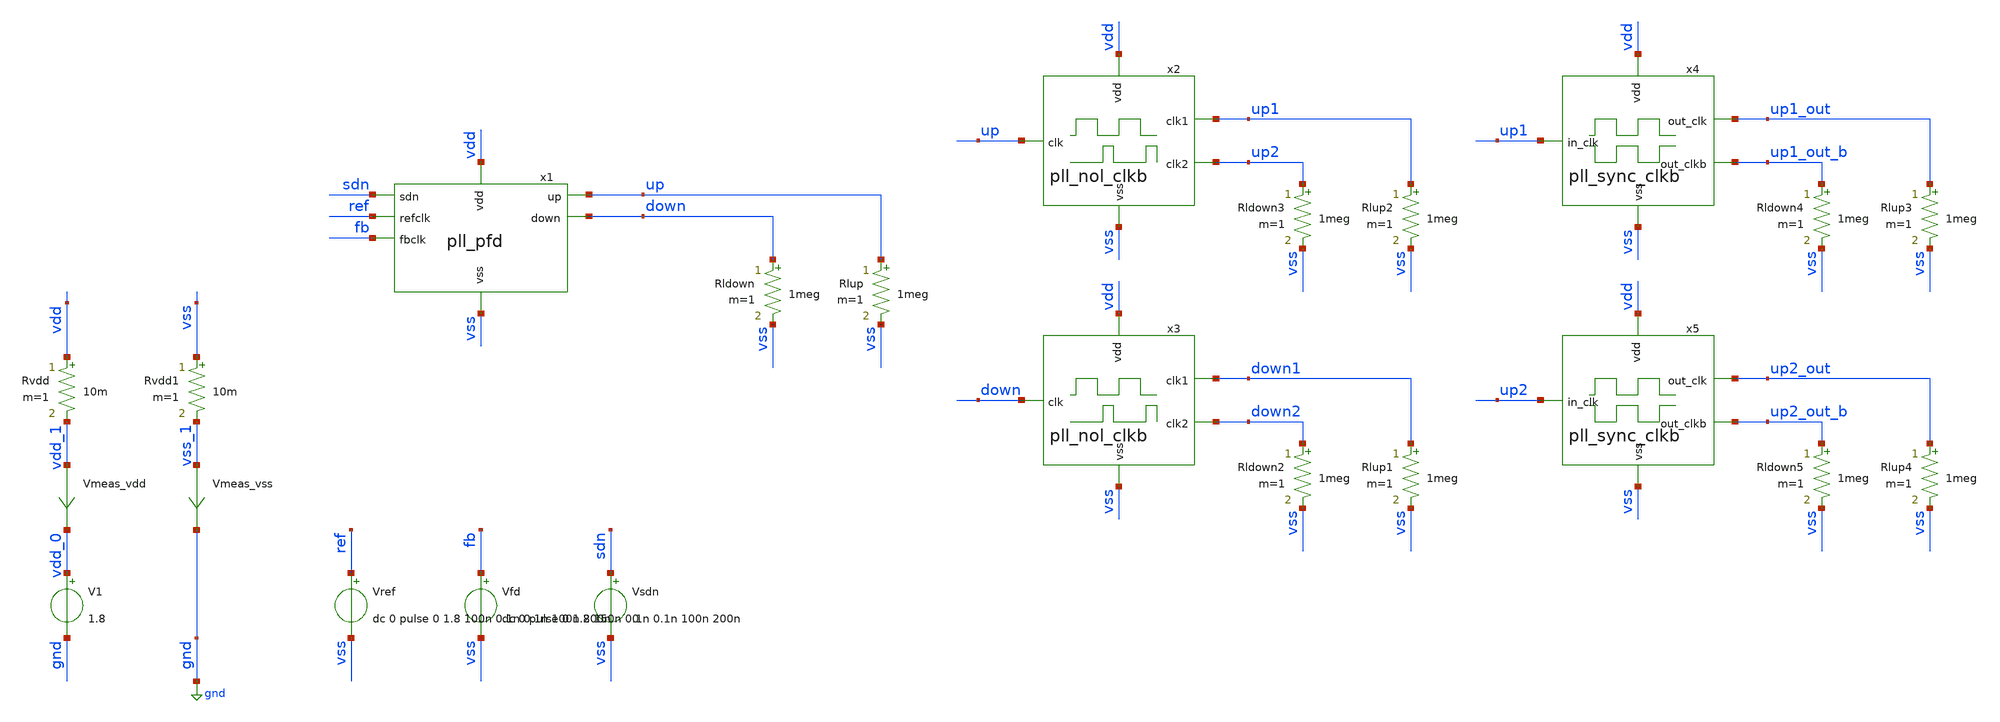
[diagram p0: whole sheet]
** sch_path: pll/pll_pfd/simulation/pll_pfd_tb.sch
**.subckt pll_pfd_tb
V1 vdd_0 gnd 1.8
Vmeas_vdd vdd_1 vdd_0 0
.save i(vmeas_vdd)
Vref ref vss dc 0 pulse 0 1.8 100n 0.1n 0.1n 100n 200n
Vfd fb vss dc 0 pulse 0 1.8 150n 0.1n 0.1n 100n 200n
Vsdn sdn vss 0
Vmeas_vss vss_1 gnd 0
.save i(vmeas_vss)
Rvdd vdd vdd_1 10m m=1
Rvdd1 vss vss_1 10m m=1
Rlup up vss 1meg m=1
Rldown down vss 1meg m=1
Rlup1 down1 vss 1meg m=1
Rldown2 down2 vss 1meg m=1
Rlup2 up1 vss 1meg m=1
Rldown3 up2 vss 1meg m=1
Rlup3 up1_out vss 1meg m=1
Rldown4 up1_out_b vss 1meg m=1
Rlup4 up2_out vss 1meg m=1
Rldown5 up2_out_b vss 1meg m=1
x1 ref up sdn fb down vdd vss pll_pfd
x2 up1 vdd vss up up2 pll_nol_clkb
x3 down1 vdd vss down down2 pll_nol_clkb
x4 up1_out vdd vss up1 up1_out_b pll_sync_clkb
x5 up2_out vdd vss up2 up2_out_b pll_sync_clkb
**** begin user architecture code



*.option savecurrents
*.option rshunt = 1e12
*.option gmin = 1e-24

** Settings for PSS osciallator
*.option reltol=1e-5
*.option vntol=3e-8
*.option abstol=1e-13
**.option chgtol=1e-12
*.option trtol=10
*.option method=gear

.control

* #################################################################
* #
* #                         OPERATING POINT
* #
* #################################################################
reset
save all

op
set filetype=binary
write pll_pfd_tb.raw all

* #################################################################
* #
* #                 TRANSIENT OSCILATION REGIME
* #
* #################################################################
reset
setplot const
save all
save v(ref)
save v(fb)
save v(sdn)
save v(up) v(up1) v(up1_out) v(up1_out_b) v(up2) v(up2_out) v(up2_out_b)
save v(down) v(down1) v(down2)
save v(x2.clkb) v(x2.clk1b) v(x2.clk1fb) v(x2.clk2b) v(x2.clk2fb)
save v(x4.stor_node) v(x4.stor_node_b)

tran 0.05n 1u
set filetype=ascii
write pll_pfd_tb_tran.raw v(ref) v(fb) v(sdn) v(up) v(up1) v(up2) v(down) v(down1) v(down2)

* Plot outputs
plot v(sdn)+16 v(ref)+14 v(fb)+12 v(up)+10 v(up1)+8 v(up2)+6 v(down)+4 v(down1)+2 v(down2)+0
plot v(up1)+10 v(up1_out)+8 v(up1_out_b)+6 v(up2)+4 v(up2_out)+2 v(up2_out_b)+0
plot v(x4.stor_node) v(x4.stor_node_b)

*rusage
.endc



.options wnflag=1
.include $::SKYWATER_MODELS/cells/nfet_01v8/sky130_fd_pr__nfet_01v8__tt.corner.spice
.include $::SKYWATER_MODELS/cells/nfet_01v8_lvt/sky130_fd_pr__nfet_01v8_lvt__tt.corner.spice
.include $::SKYWATER_MODELS/cells/pfet_01v8/sky130_fd_pr__pfet_01v8__tt.corner.spice
.include $::SKYWATER_MODELS/cells/nfet_03v3_nvt/sky130_fd_pr__nfet_03v3_nvt__tt.corner.spice
.include $::SKYWATER_MODELS/cells/nfet_05v0_nvt/sky130_fd_pr__nfet_05v0_nvt__tt.corner.spice
.include $::SKYWATER_MODELS/cells/esd_nfet_01v8/sky130_fd_pr__esd_nfet_01v8__tt.corner.spice
.include $::SKYWATER_MODELS/cells/pfet_01v8_lvt/sky130_fd_pr__pfet_01v8_lvt__tt.corner.spice
.include $::SKYWATER_MODELS/cells/pfet_01v8_hvt/sky130_fd_pr__pfet_01v8_hvt__tt.corner.spice
.include $::SKYWATER_MODELS/cells/esd_pfet_g5v0d10v5/sky130_fd_pr__esd_pfet_g5v0d10v5__tt.corner.spice
.include $::SKYWATER_MODELS/cells/pfet_g5v0d10v5/sky130_fd_pr__pfet_g5v0d10v5__tt.corner.spice
.include $::SKYWATER_MODELS/cells/pfet_g5v0d16v0/sky130_fd_pr__pfet_g5v0d16v0__tt.corner.spice
.include $::SKYWATER_MODELS/cells/nfet_g5v0d10v5/sky130_fd_pr__nfet_g5v0d10v5__tt.corner.spice
.include $::SKYWATER_MODELS/cells/nfet_g5v0d16v0/sky130_fd_pr__nfet_g5v0d16v0__tt_discrete.corner.spice
.include $::SKYWATER_MODELS/cells/esd_nfet_g5v0d10v5/sky130_fd_pr__esd_nfet_g5v0d10v5__tt.corner.spice
.include $::SKYWATER_MODELS/models/corners/tt/nonfet.spice

.include $::SKYWATER_MODELS/cells/cap_var_hvt/sky130_fd_pr__cap_var_hvt.model.spice

* Mismatch parameters
.include $::SKYWATER_MODELS/cells/nfet_01v8/sky130_fd_pr__nfet_01v8__mismatch.corner.spice
.include $::SKYWATER_MODELS/cells/pfet_01v8/sky130_fd_pr__pfet_01v8__mismatch.corner.spice
.include $::SKYWATER_MODELS/cells/nfet_01v8_lvt/sky130_fd_pr__nfet_01v8_lvt__mismatch.corner.spice
.include $::SKYWATER_MODELS/cells/pfet_01v8_lvt/sky130_fd_pr__pfet_01v8_lvt__mismatch.corner.spice
.include $::SKYWATER_MODELS/cells/pfet_01v8_hvt/sky130_fd_pr__pfet_01v8_hvt__mismatch.corner.spice
.include $::SKYWATER_MODELS/cells/nfet_g5v0d10v5/sky130_fd_pr__nfet_g5v0d10v5__mismatch.corner.spice
.include $::SKYWATER_MODELS/cells/pfet_g5v0d10v5/sky130_fd_pr__pfet_g5v0d10v5__mismatch.corner.spice
.include $::SKYWATER_MODELS/cells/nfet_05v0_nvt/sky130_fd_pr__nfet_05v0_nvt__mismatch.corner.spice
.include $::SKYWATER_MODELS/cells/nfet_03v3_nvt/sky130_fd_pr__nfet_03v3_nvt__mismatch.corner.spice

* Resistor$::SKYWATER_MODELS/Capacitor
.include $::SKYWATER_MODELS/models/r+c/res_typical__cap_typical.spice
.include $::SKYWATER_MODELS/models/r+c/res_typical__cap_typical__lin.spice

* Special cells
.include $::SKYWATER_MODELS/models/corners/tt/specialized_cells.spice

* All models
.include $::SKYWATER_MODELS/models/all.spice

* Corner
.include $::SKYWATER_MODELS/models/corners/tt/rf.spice

* .include $::SKYWATER_STDCELLS/cells/
.include $::SKYWATER_STDCELLS/cells/buf/sky130_fd_sc_hd__buf_1.spice
.include $::SKYWATER_STDCELLS_HS/cells/buf/sky130_fd_sc_hs__buf_1.spice
.include $::SKYWATER_STDCELLS_HS/cells/buf/sky130_fd_sc_hs__buf_16.spice
.include $::SKYWATER_STDCELLS/cells/clkbuf/sky130_fd_sc_hd__clkbuf_1.spice
.include $::SKYWATER_STDCELLS/cells/clkbuf/sky130_fd_sc_hd__clkbuf_2.spice
.include $::SKYWATER_STDCELLS/cells/clkbuf/sky130_fd_sc_hd__clkbuf_4.spice
.include $::SKYWATER_STDCELLS/cells/clkbuf/sky130_fd_sc_hd__clkbuf_8.spice
.include $::SKYWATER_STDCELLS/cells/clkbuf/sky130_fd_sc_hd__clkbuf_16.spice
.include $::SKYWATER_STDCELLS/cells/decap/sky130_fd_sc_hd__decap_3.spice
.include $::SKYWATER_STDCELLS/cells/decap/sky130_fd_sc_hd__decap_4.spice
.include $::SKYWATER_STDCELLS/cells/decap/sky130_fd_sc_hd__decap_8.spice
.include $::SKYWATER_STDCELLS/cells/dfrbp/sky130_fd_sc_hd__dfrbp_1.spice
.include $::SKYWATER_STDCELLS/cells/dfrbp/sky130_fd_sc_hd__dfrbp_2.spice
.include $::SKYWATER_STDCELLS/cells/inv/sky130_fd_sc_hd__inv_1.spice
.include $::SKYWATER_STDCELLS/cells/inv/sky130_fd_sc_hd__inv_2.spice
.include $::SKYWATER_STDCELLS/cells/inv/sky130_fd_sc_hd__inv_4.spice
.include $::SKYWATER_STDCELLS/cells/inv/sky130_fd_sc_hd__inv_8.spice
.include $::SKYWATER_STDCELLS/cells/inv/sky130_fd_sc_hd__inv_16.spice
.include $::SKYWATER_STDCELLS_HS/cells/inv/sky130_fd_sc_hs__inv_1.spice
.include $::SKYWATER_STDCELLS_HS/cells/inv/sky130_fd_sc_hs__inv_2.spice
.include $::SKYWATER_STDCELLS_HS/cells/inv/sky130_fd_sc_hs__inv_4.spice
.include $::SKYWATER_STDCELLS_HS/cells/inv/sky130_fd_sc_hs__inv_8.spice
.include $::SKYWATER_STDCELLS_HS/cells/inv/sky130_fd_sc_hs__inv_16.spice
.include $::SKYWATER_STDCELLS/cells/mux2/sky130_fd_sc_hd__mux2_2.spice
.include $::SKYWATER_STDCELLS/cells/nand2/sky130_fd_sc_hd__nand2_1.spice
.include $::SKYWATER_STDCELLS/cells/tap/sky130_fd_sc_hd__tap_2.spice
.include $::SKYWATER_STDCELLS/cells/tapvpwrvgnd/sky130_fd_sc_hd__tapvpwrvgnd_1.spice

**** end user architecture code
**.ends

* expanding   symbol:  test_jens/pll/pll_pfd/pll_pfd.sym # of pins=7
** sym_path: pll/pll_pfd/xschem/pll_pfd.sym
** sch_path: pll/pll_pfd/xschem/pll_pfd.sch
.subckt pll_pfd refclk up sdn fbclk down vdd vss
*.ipin refclk
*.ipin fbclk
*.opin up
*.opin down
*.ipin sdn
*.ipin vdd
*.ipin vss
x1 refclk vdd rst_3 vss vss vdd vdd up up_inv sky130_fd_sc_hd__dfrbp_2
x2 fbclk vdd rst_3 vss vss vdd vdd down down_inv sky130_fd_sc_hd__dfrbp_2
x6 rst_2 sdn_inv vss vss vdd vdd rst_3 sky130_fd_sc_hd__and2_2
x4 rst_0 vss vss vdd vdd rst_1 sky130_fd_sc_hd__buf_1
x5 rst_1 vss vss vdd vdd rst_2 sky130_fd_sc_hd__buf_1
x7 sdn vss vss vdd vdd sdn_inv sky130_fd_sc_hd__inv_1
**** begin user architecture code
* .include $::SKYWATER_STDCELLS/cells/
.include $::SKYWATER_STDCELLS/cells/and2/sky130_fd_sc_hd__and2_1.spice
.include $::SKYWATER_STDCELLS/cells/and2/sky130_fd_sc_hd__and2_2.spice
.include $::SKYWATER_STDCELLS_HS/cells/and2/sky130_fd_sc_hs__and2_1.spice
.include $::SKYWATER_STDCELLS_HS/cells/and2/sky130_fd_sc_hs__and2_2.spice

.include $::SKYWATER_STDCELLS/cells/or2/sky130_fd_sc_hd__or2_1.spice
.include $::SKYWATER_STDCELLS/cells/or2/sky130_fd_sc_hd__or2_2.spice
.include $::SKYWATER_STDCELLS_HS/cells/or2/sky130_fd_sc_hs__or2_1.spice
.include $::SKYWATER_STDCELLS_HS/cells/or2/sky130_fd_sc_hs__or2_2.spice

.include $::SKYWATER_STDCELLS/cells/buf/sky130_fd_sc_hd__buf_1.spice
.include $::SKYWATER_STDCELLS_HS/cells/buf/sky130_fd_sc_hs__buf_1.spice

.include $::SKYWATER_STDCELLS/cells/dfrbp/sky130_fd_sc_hd__dfrbp_1.spice
.include $::SKYWATER_STDCELLS/cells/dfrbp/sky130_fd_sc_hd__dfrbp_2.spice
.include $::SKYWATER_STDCELLS_HS/cells/dfrbp/sky130_fd_sc_hs__dfrbp_1.spice
.include $::SKYWATER_STDCELLS_HS/cells/dfrbp/sky130_fd_sc_hs__dfrbp_2.spice

.include $::SKYWATER_STDCELLS/cells/inv/sky130_fd_sc_hd__inv_1.spice
.include $::SKYWATER_STDCELLS/cells/inv/sky130_fd_sc_hd__inv_2.spice
.include $::SKYWATER_STDCELLS/cells/inv/sky130_fd_sc_hd__inv_4.spice
.include $::SKYWATER_STDCELLS/cells/inv/sky130_fd_sc_hd__inv_8.spice
.include $::SKYWATER_STDCELLS/cells/inv/sky130_fd_sc_hd__inv_16.spice
.include $::SKYWATER_STDCELLS_HS/cells/inv/sky130_fd_sc_hs__inv_1.spice
.include $::SKYWATER_STDCELLS_HS/cells/inv/sky130_fd_sc_hs__inv_2.spice
.include $::SKYWATER_STDCELLS_HS/cells/inv/sky130_fd_sc_hs__inv_4.spice
.include $::SKYWATER_STDCELLS_HS/cells/inv/sky130_fd_sc_hs__inv_8.spice
.include $::SKYWATER_STDCELLS_HS/cells/inv/sky130_fd_sc_hs__inv_16.spice

.include $::SKYWATER_STDCELLS/cells/mux2/sky130_fd_sc_hd__mux2_2.spice
.include $::SKYWATER_STDCELLS/cells/nand2/sky130_fd_sc_hd__nand2_1.spice

.include $::SKYWATER_STDCELLS/cells/tap/sky130_fd_sc_hd__tap_2.spice
.include $::SKYWATER_STDCELLS/cells/tapvpwrvgnd/sky130_fd_sc_hd__tapvpwrvgnd_1.spice

**** end user architecture code
x3 up_inv down_inv vss vss vdd vdd rst_0 sky130_fd_sc_hd__or2_1
* noconn vss
* noconn vdd
.ends


* expanding   symbol:  test_jens/pll/pll_nol_clkb/pll_nol_clkb.sym # of pins=5
** sym_path: pll/pll_nol_clkb/xschem/pll_nol_clkb.sym
** sch_path: pll/pll_nol_clkb/xschem/pll_nol_clkb.sch
.subckt pll_nol_clkb clk1 vdd vss clk clk2
*.opin clk1
*.opin clk2
*.ipin vdd
*.ipin vss
*.ipin clk
**** begin user architecture code
* .include $::SKYWATER_STDCELLS/cells/
.include $::SKYWATER_STDCELLS/cells/and2/sky130_fd_sc_hd__and2_1.spice
.include $::SKYWATER_STDCELLS/cells/and2/sky130_fd_sc_hd__and2_2.spice
.include $::SKYWATER_STDCELLS_HS/cells/and2/sky130_fd_sc_hs__and2_1.spice
.include $::SKYWATER_STDCELLS_HS/cells/and2/sky130_fd_sc_hs__and2_2.spice

.include $::SKYWATER_STDCELLS/cells/nand2/sky130_fd_sc_hd__nand2_1.spice
.include $::SKYWATER_STDCELLS/cells/nand2/sky130_fd_sc_hd__nand2_2.spice
.include $::SKYWATER_STDCELLS_HS/cells/nand2/sky130_fd_sc_hs__nand2_1.spice
.include $::SKYWATER_STDCELLS_HS/cells/nand2/sky130_fd_sc_hs__nand2_2.spice

.include $::SKYWATER_STDCELLS/cells/or2/sky130_fd_sc_hd__or2_1.spice
.include $::SKYWATER_STDCELLS/cells/or2/sky130_fd_sc_hd__or2_2.spice
.include $::SKYWATER_STDCELLS_HS/cells/or2/sky130_fd_sc_hs__or2_1.spice
.include $::SKYWATER_STDCELLS_HS/cells/or2/sky130_fd_sc_hs__or2_2.spice

.include $::SKYWATER_STDCELLS/cells/buf/sky130_fd_sc_hd__buf_1.spice
.include $::SKYWATER_STDCELLS_HS/cells/buf/sky130_fd_sc_hs__buf_1.spice

.include $::SKYWATER_STDCELLS/cells/dfrbp/sky130_fd_sc_hd__dfrbp_1.spice
.include $::SKYWATER_STDCELLS/cells/dfrbp/sky130_fd_sc_hd__dfrbp_2.spice
.include $::SKYWATER_STDCELLS_HS/cells/dfrbp/sky130_fd_sc_hs__dfrbp_1.spice
.include $::SKYWATER_STDCELLS_HS/cells/dfrbp/sky130_fd_sc_hs__dfrbp_2.spice

.include $::SKYWATER_STDCELLS/cells/inv/sky130_fd_sc_hd__inv_1.spice
.include $::SKYWATER_STDCELLS/cells/inv/sky130_fd_sc_hd__inv_2.spice
.include $::SKYWATER_STDCELLS/cells/inv/sky130_fd_sc_hd__inv_4.spice
.include $::SKYWATER_STDCELLS/cells/inv/sky130_fd_sc_hd__inv_8.spice
.include $::SKYWATER_STDCELLS/cells/inv/sky130_fd_sc_hd__inv_16.spice
.include $::SKYWATER_STDCELLS_HS/cells/inv/sky130_fd_sc_hs__inv_1.spice
.include $::SKYWATER_STDCELLS_HS/cells/inv/sky130_fd_sc_hs__inv_2.spice
.include $::SKYWATER_STDCELLS_HS/cells/inv/sky130_fd_sc_hs__inv_4.spice
.include $::SKYWATER_STDCELLS_HS/cells/inv/sky130_fd_sc_hs__inv_8.spice
.include $::SKYWATER_STDCELLS_HS/cells/inv/sky130_fd_sc_hs__inv_16.spice

.include $::SKYWATER_STDCELLS/cells/mux2/sky130_fd_sc_hd__mux2_2.spice
.include $::SKYWATER_STDCELLS/cells/nand2/sky130_fd_sc_hd__nand2_1.spice

.include $::SKYWATER_STDCELLS/cells/tap/sky130_fd_sc_hd__tap_2.spice
.include $::SKYWATER_STDCELLS/cells/tapvpwrvgnd/sky130_fd_sc_hd__tapvpwrvgnd_1.spice

**** end user architecture code
x3 clk1b vss vss vdd vdd clk1 sky130_fd_sc_hd__inv_1
x4 clk1 vss vss vdd vdd clk1fb sky130_fd_sc_hd__inv_1
x5 clk2b vss vss vdd vdd clk2 sky130_fd_sc_hd__inv_1
x6 clk2 vss vss vdd vdd clk2fb sky130_fd_sc_hd__inv_1
x7 clk vss vss vdd vdd clkb sky130_fd_sc_hd__inv_1
x1 clkb clk2fb vss vss vdd vdd clk1b sky130_fd_sc_hd__nand2_2
x2 clk1fb clk vss vss vdd vdd clk2b sky130_fd_sc_hd__nand2_2
* noconn vdd
* noconn vss
.ends


* expanding   symbol:  test_jens/pll/pll_sync_clkb/pll_sync_clkb.sym # of pins=5
** sym_path: pll/pll_sync_clkb/xschem/pll_sync_clkb.sym
** sch_path: pll/pll_sync_clkb/xschem/pll_sync_clkb.sch
.subckt pll_sync_clkb out_clk vdd vss in_clk out_clkb
*.opin out_clk
*.opin out_clkb
*.ipin vdd
*.ipin vss
*.ipin in_clk
**** begin user architecture code
* .include $::SKYWATER_STDCELLS/cells/
.include $::SKYWATER_STDCELLS/cells/and2/sky130_fd_sc_hd__and2_1.spice
.include $::SKYWATER_STDCELLS/cells/and2/sky130_fd_sc_hd__and2_2.spice
.include $::SKYWATER_STDCELLS_HS/cells/and2/sky130_fd_sc_hs__and2_1.spice
.include $::SKYWATER_STDCELLS_HS/cells/and2/sky130_fd_sc_hs__and2_2.spice

.include $::SKYWATER_STDCELLS/cells/nand2/sky130_fd_sc_hd__nand2_1.spice
.include $::SKYWATER_STDCELLS/cells/nand2/sky130_fd_sc_hd__nand2_2.spice
.include $::SKYWATER_STDCELLS_HS/cells/nand2/sky130_fd_sc_hs__nand2_1.spice
.include $::SKYWATER_STDCELLS_HS/cells/nand2/sky130_fd_sc_hs__nand2_2.spice

.include $::SKYWATER_STDCELLS/cells/or2/sky130_fd_sc_hd__or2_1.spice
.include $::SKYWATER_STDCELLS/cells/or2/sky130_fd_sc_hd__or2_2.spice
.include $::SKYWATER_STDCELLS_HS/cells/or2/sky130_fd_sc_hs__or2_1.spice
.include $::SKYWATER_STDCELLS_HS/cells/or2/sky130_fd_sc_hs__or2_2.spice

.include $::SKYWATER_STDCELLS/cells/buf/sky130_fd_sc_hd__buf_1.spice
.include $::SKYWATER_STDCELLS_HS/cells/buf/sky130_fd_sc_hs__buf_1.spice

.include $::SKYWATER_STDCELLS/cells/dfrbp/sky130_fd_sc_hd__dfrbp_1.spice
.include $::SKYWATER_STDCELLS/cells/dfrbp/sky130_fd_sc_hd__dfrbp_2.spice
.include $::SKYWATER_STDCELLS_HS/cells/dfrbp/sky130_fd_sc_hs__dfrbp_1.spice
.include $::SKYWATER_STDCELLS_HS/cells/dfrbp/sky130_fd_sc_hs__dfrbp_2.spice

.include $::SKYWATER_STDCELLS/cells/inv/sky130_fd_sc_hd__inv_1.spice
.include $::SKYWATER_STDCELLS/cells/inv/sky130_fd_sc_hd__inv_2.spice
.include $::SKYWATER_STDCELLS/cells/inv/sky130_fd_sc_hd__inv_4.spice
.include $::SKYWATER_STDCELLS/cells/inv/sky130_fd_sc_hd__inv_8.spice
.include $::SKYWATER_STDCELLS/cells/inv/sky130_fd_sc_hd__inv_16.spice
.include $::SKYWATER_STDCELLS_HS/cells/inv/sky130_fd_sc_hs__inv_1.spice
.include $::SKYWATER_STDCELLS_HS/cells/inv/sky130_fd_sc_hs__inv_2.spice
.include $::SKYWATER_STDCELLS_HS/cells/inv/sky130_fd_sc_hs__inv_4.spice
.include $::SKYWATER_STDCELLS_HS/cells/inv/sky130_fd_sc_hs__inv_8.spice
.include $::SKYWATER_STDCELLS_HS/cells/inv/sky130_fd_sc_hs__inv_16.spice

.include $::SKYWATER_STDCELLS/cells/mux2/sky130_fd_sc_hd__mux2_2.spice
.include $::SKYWATER_STDCELLS/cells/nand2/sky130_fd_sc_hd__nand2_1.spice

.include $::SKYWATER_STDCELLS/cells/tap/sky130_fd_sc_hd__tap_2.spice
.include $::SKYWATER_STDCELLS/cells/tapvpwrvgnd/sky130_fd_sc_hd__tapvpwrvgnd_1.spice

**** end user architecture code
x1 in_clk vss vss vdd vdd net1 sky130_fd_sc_hd__inv_2
x2 net1 vss vss vdd vdd net2 sky130_fd_sc_hd__inv_2
x4 stor_node vss vss vdd vdd out_clk sky130_fd_sc_hd__inv_1
x6 stor_node_b vss vss vdd vdd out_clkb sky130_fd_sc_hd__inv_1
x7 stor_node_b vss vss vdd vdd stor_node sky130_fd_sc_hd__inv_2
x9 stor_node vss vss vdd vdd stor_node_b sky130_fd_sc_hd__inv_2
x3 net2 vss vss vdd vdd stor_node sky130_fd_sc_hd__inv_1
x5 net1 vss vss vdd vdd stor_node_b sky130_fd_sc_hd__inv_1
* noconn vdd
* noconn vss
.ends

.GLOBAL gnd
.end
